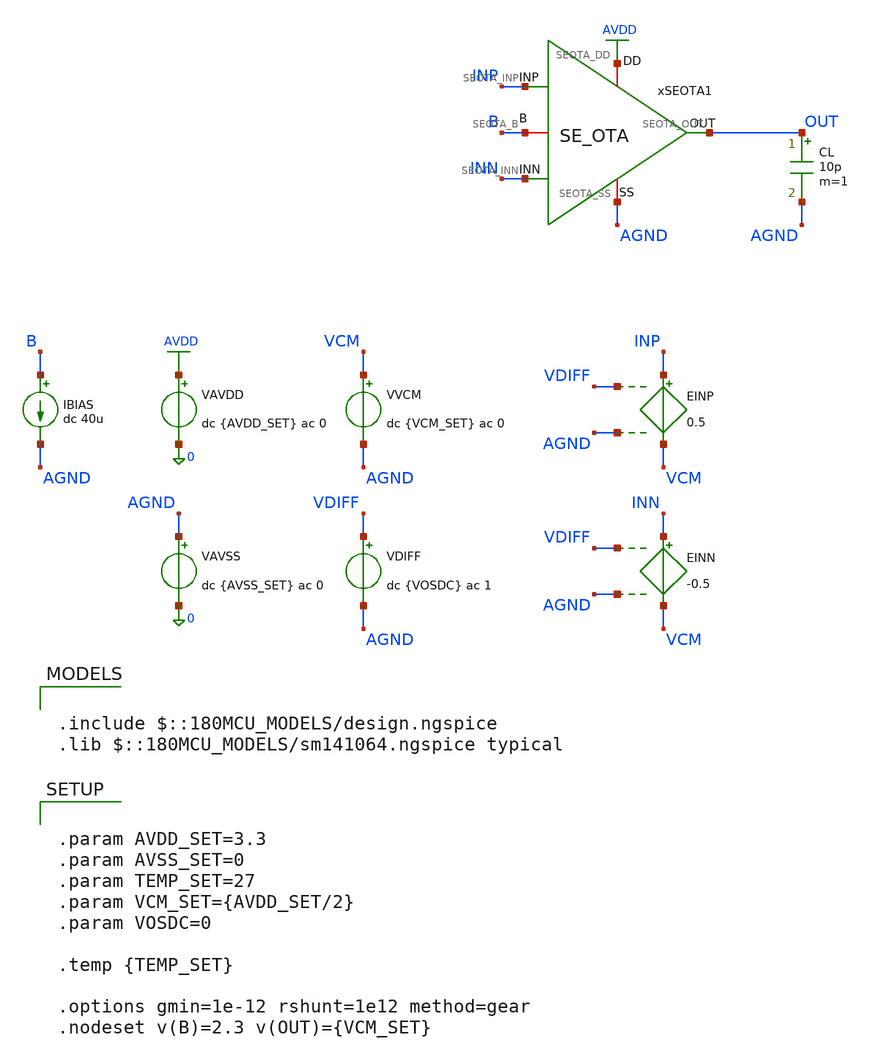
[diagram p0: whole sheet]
** sch_path: Design_Files/IC Design/Testbench/SE_OTA/Open_Loop_Noise/SE_OTA_TB_OL_NOISE_NOM.sch
**.subckt SE_OTA_TB_OL_NOISE_NOM
IBIAS B AGND dc 40u
VAVDD AVDD 0 dc {AVDD_SET} ac 0
.save i(vavdd)
CL OUT AGND 10p m=1
VVCM VCM AGND dc {VCM_SET} ac 0
VDIFF VDIFF AGND dc {VOSDC} ac 1
xSEOTA1 AVDD AGND INP INN OUT B SE_OTA
VAVSS AGND 0 dc {AVSS_SET} ac 0
.save i(vavss)
EINN INN VCM VDIFF AGND -0.5
EINP INP VCM VDIFF AGND 0.5
**** begin user architecture code

.include $::180MCU_MODELS/design.ngspice
.lib $::180MCU_MODELS/sm141064.ngspice typical



.param AVDD_SET=3.3
.param AVSS_SET=0
.param TEMP_SET=27
.param VCM_SET={AVDD_SET/2}
.param VOSDC=0

.temp {TEMP_SET}

.options gmin=1e-12 rshunt=1e12 method=gear
.nodeset v(B)=2.3 v(OUT)={VCM_SET}




.control
destroy all
save all
set wr_vecnames
set wr_singlescale
unset sqrnoise

shell mkdir -p
+ /foss/designs/ECG_Acquisition_IC/Measurement_Results/IC_Simulation/SE_OTA/NOM.Result_txt

shell rm -f
+ /foss/designs/ECG_Acquisition_IC/Measurement_Results/IC_Simulation/SE_OTA/NOM.Result_txt/NOM.noise_spectrum.txt
shell rm -f
+ /foss/designs/ECG_Acquisition_IC/Measurement_Results/IC_Simulation/SE_OTA/NOM.Result_txt/NOM.noise_total.txt

* set this from offset
let vos_run = 0

alter @VDIFF[DC] = $&vos_run
alter @VDIFF[ACMAG] = 1
alter @VVCM[ACMAG] = 0
alter @VAVDD[ACMAG] = 0
alter @VAVSS[ACMAG] = 0

* Noise
noise v(out) VDIFF dec 100 0.05 150

setplot noise1
let in_noise  = inoise_spectrum
let out_noise = onoise_spectrum

wrdata
+ /foss/designs/ECG_Acquisition_IC/Measurement_Results/IC_Simulation/SE_OTA/NOM.Result_txt/NOM.noise_spectrum.txt in_noise out_noise

setplot noise2
let fmin = 0.05
let fmax = 150
let in_total  = inoise_total
let out_total = onoise_total

wrdata
+ /foss/designs/ECG_Acquisition_IC/Measurement_Results/IC_Simulation/SE_OTA/NOM.Result_txt/NOM.noise_total.txt fmin fmax in_total out_total

.endc


**** end user architecture code
**.ends

* expanding   symbol:  ECG_Acquisition_IC/Design_Files/IC Design/Schematic/SE_OTA/SE_OTA.sym # of
*+ pins=6
** sym_path: Design_Files/IC Design/Schematic/SE_OTA/SE_OTA.sym
** sch_path: Design_Files/IC Design/Schematic/SE_OTA/SE_OTA.sch
.subckt SE_OTA SEOTA_DD SEOTA_SS SEOTA_INP SEOTA_INN SEOTA_OUT SEOTA_B
*.iopin SEOTA_DD
*.iopin SEOTA_SS
*.ipin SEOTA_INP
*.ipin SEOTA_INN
*.opin SEOTA_OUT
*.iopin SEOTA_B
XM3 net4 net4 SEOTA_DD SEOTA_DD pfet_03v3 L=4u W=1u nf=1 ad='int((nf+1)/2) * W/nf * 0.18u' as='int((nf+2)/2) * W/nf * 0.18u'
+ pd='2*int((nf+1)/2) * (W/nf + 0.18u)' ps='2*int((nf+2)/2) * (W/nf + 0.18u)' nrd='0.18u / W' nrs='0.18u / W'
+ sa=0 sb=0 sd=0 m=60
XM7 SEOTA_OUT SEOTA_B SEOTA_SS SEOTA_SS nfet_03v3 L=0.5u W=1u nf=1 ad='int((nf+1)/2) * W/nf * 0.18u'
+ as='int((nf+2)/2) * W/nf * 0.18u' pd='2*int((nf+1)/2) * (W/nf + 0.18u)' ps='2*int((nf+2)/2) * (W/nf + 0.18u)'
+ nrd='0.18u / W' nrs='0.18u / W' sa=0 sb=0 sd=0 m=100
Rz net1 net2 3.8k m=1
XM5 net3 SEOTA_B SEOTA_SS SEOTA_SS nfet_03v3 L=2u W=1u nf=1 ad='int((nf+1)/2) * W/nf * 0.18u' as='int((nf+2)/2) * W/nf * 0.18u'
+ pd='2*int((nf+1)/2) * (W/nf + 0.18u)' ps='2*int((nf+2)/2) * (W/nf + 0.18u)' nrd='0.18u / W' nrs='0.18u / W'
+ sa=0 sb=0 sd=0 m=10
XM6 SEOTA_OUT net1 SEOTA_DD SEOTA_DD pfet_03v3 L=0.5u W=1u nf=1 ad='int((nf+1)/2) * W/nf * 0.18u' as='int((nf+2)/2) * W/nf * 0.18u'
+ pd='2*int((nf+1)/2) * (W/nf + 0.18u)' ps='2*int((nf+2)/2) * (W/nf + 0.18u)' nrd='0.18u / W' nrs='0.18u / W'
+ sa=0 sb=0 sd=0 m=400
XM8 SEOTA_B SEOTA_B SEOTA_SS SEOTA_SS nfet_03v3 L=2u W=1u nf=1 ad='int((nf+1)/2) * W/nf * 0.18u' as='int((nf+2)/2) * W/nf * 0.18u'
+ pd='2*int((nf+1)/2) * (W/nf + 0.18u)' ps='2*int((nf+2)/2) * (W/nf + 0.18u)' nrd='0.18u / W' nrs='0.18u / W'
+ sa=0 sb=0 sd=0 m=20
Cc net2 SEOTA_OUT 2p m=1
XM4 net1 net4 SEOTA_DD SEOTA_DD pfet_03v3 L=4u W=1u nf=1 ad='int((nf+1)/2) * W/nf * 0.18u' as='int((nf+2)/2) * W/nf * 0.18u'
+ pd='2*int((nf+1)/2) * (W/nf + 0.18u)' ps='2*int((nf+2)/2) * (W/nf + 0.18u)' nrd='0.18u / W' nrs='0.18u / W'
+ sa=0 sb=0 sd=0 m=60
XM1 net4 SEOTA_INN net3 SEOTA_SS nfet_03v3 L=4u W=1u nf=1 ad='int((nf+1)/2) * W/nf * 0.18u' as='int((nf+2)/2) * W/nf * 0.18u'
+ pd='2*int((nf+1)/2) * (W/nf + 0.18u)' ps='2*int((nf+2)/2) * (W/nf + 0.18u)' nrd='0.18u / W' nrs='0.18u / W'
+ sa=0 sb=0 sd=0 m=400
XM2 net1 SEOTA_INP net3 SEOTA_SS nfet_03v3 L=4u W=1u nf=1 ad='int((nf+1)/2) * W/nf * 0.18u' as='int((nf+2)/2) * W/nf * 0.18u'
+ pd='2*int((nf+1)/2) * (W/nf + 0.18u)' ps='2*int((nf+2)/2) * (W/nf + 0.18u)' nrd='0.18u / W' nrs='0.18u / W'
+ sa=0 sb=0 sd=0 m=400
.ends

.GLOBAL AVDD
.end
